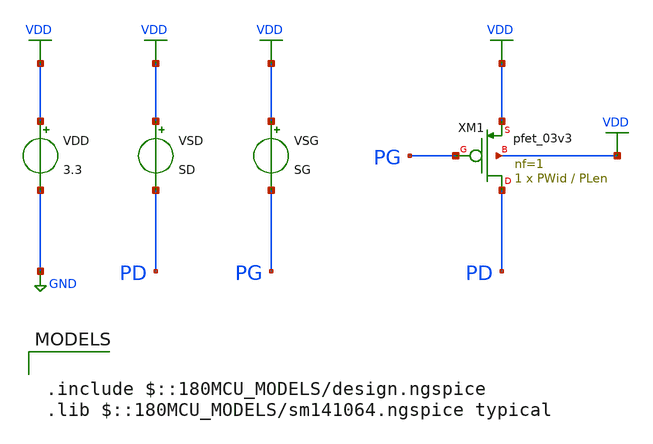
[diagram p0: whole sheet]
** sch_path: Design_Files/IC Design/Testbench/SIZING/Gm_Id/PMOS_Gm_Id.sch
**.subckt PMOS_Gm_Id
XM1 PD PG VDD VDD pfet_03v3 L=PLen W=PWid nf=1 ad='int((nf+1)/2) * W/nf * 0.18u' as='int((nf+2)/2) * W/nf * 0.18u'
+ pd='2*int((nf+1)/2) * (W/nf + 0.18u)' ps='2*int((nf+2)/2) * (W/nf + 0.18u)' nrd='0.18u / W' nrs='0.18u / W'
+ sa=0 sb=0 sd=0 m=1
VSG VDD PG SG
VSD VDD PD SD
.save i(vsd)
VDD VDD GND 3.3
**** begin user architecture code



.param PWid=10u
.param PLen=1u
.param SG=0
.param SD=1.65

.control

shell mkdir -p
+ /foss/designs/ECG_Acquisition_IC/Measurement_Results/IC_Simulation/SIZING/Gm_Id/PMOS_Gm_Id/Results_txt

set wr_vecnames
set wr_singlescale

* =========================================================
* PMOS gm/Id + fT 2D DC sweep
* W fixed at 10u
* VSG: 0 to 3.3 V
* VSD: 0 to 3.3 V
* Export: VSG VSD ID ID/W gm gds Cgs Cgd Cgb Cgg fT
* =========================================================

alterparam PLen = 0.28u
reset
save v(vdd) v(pg) v(pd) vsd#branch @m.xm1.m0[gm] @m.xm1.m0[gds] @m.xm1.m0[cgs] @m.xm1.m0[cgd]
+ @m.xm1.m0[cgb]
dc VSG 0 3.3 0.01 VSD 0 3.3 0.05
let vsg_out = v(vdd)-v(pg)
let vsd_out = v(vdd)-v(pd)
let id = abs(vsd#branch)
let id_w = id/10e-6
let gm = abs(@m.xm1.m0[gm])
let gds = abs(@m.xm1.m0[gds])
let cgs = abs(@m.xm1.m0[cgs])
let cgd = abs(@m.xm1.m0[cgd])
let cgb = abs(@m.xm1.m0[cgb])
let cgg = cgs + cgd + cgb
let ft_hz = gm/(6.283185307179586*(cgg + 1e-30))
let ft_mhz = ft_hz/1e6
wrdata
+ /foss/designs/ECG_Acquisition_IC/Measurement_Results/IC_Simulation/SIZING/Gm_Id/PMOS_Gm_Id/Results_txt/pmos_L0p28u_W10u.txt vsg_out vsd_out id id_w gm gds cgs cgd cgb cgg ft_hz ft_mhz

alterparam PLen = 0.5u
reset
save v(vdd) v(pg) v(pd) vsd#branch @m.xm1.m0[gm] @m.xm1.m0[gds] @m.xm1.m0[cgs] @m.xm1.m0[cgd]
+ @m.xm1.m0[cgb]
dc VSG 0 3.3 0.01 VSD 0 3.3 0.05
let vsg_out = v(vdd)-v(pg)
let vsd_out = v(vdd)-v(pd)
let id = abs(vsd#branch)
let id_w = id/10e-6
let gm = abs(@m.xm1.m0[gm])
let gds = abs(@m.xm1.m0[gds])
let cgs = abs(@m.xm1.m0[cgs])
let cgd = abs(@m.xm1.m0[cgd])
let cgb = abs(@m.xm1.m0[cgb])
let cgg = cgs + cgd + cgb
let ft_hz = gm/(6.283185307179586*(cgg + 1e-30))
let ft_mhz = ft_hz/1e6
wrdata
+ /foss/designs/ECG_Acquisition_IC/Measurement_Results/IC_Simulation/SIZING/Gm_Id/PMOS_Gm_Id/Results_txt/pmos_L0p5u_W10u.txt vsg_out vsd_out id id_w gm gds cgs cgd cgb cgg ft_hz ft_mhz

alterparam PLen = 1u
reset
save v(vdd) v(pg) v(pd) vsd#branch @m.xm1.m0[gm] @m.xm1.m0[gds] @m.xm1.m0[cgs] @m.xm1.m0[cgd]
+ @m.xm1.m0[cgb]
dc VSG 0 3.3 0.01 VSD 0 3.3 0.05
let vsg_out = v(vdd)-v(pg)
let vsd_out = v(vdd)-v(pd)
let id = abs(vsd#branch)
let id_w = id/10e-6
let gm = abs(@m.xm1.m0[gm])
let gds = abs(@m.xm1.m0[gds])
let cgs = abs(@m.xm1.m0[cgs])
let cgd = abs(@m.xm1.m0[cgd])
let cgb = abs(@m.xm1.m0[cgb])
let cgg = cgs + cgd + cgb
let ft_hz = gm/(6.283185307179586*(cgg + 1e-30))
let ft_mhz = ft_hz/1e6
wrdata
+ /foss/designs/ECG_Acquisition_IC/Measurement_Results/IC_Simulation/SIZING/Gm_Id/PMOS_Gm_Id/Results_txt/pmos_L1u_W10u.txt vsg_out vsd_out id id_w gm gds cgs cgd cgb cgg ft_hz ft_mhz

alterparam PLen = 1.5u
reset
save v(vdd) v(pg) v(pd) vsd#branch @m.xm1.m0[gm] @m.xm1.m0[gds] @m.xm1.m0[cgs] @m.xm1.m0[cgd]
+ @m.xm1.m0[cgb]
dc VSG 0 3.3 0.01 VSD 0 3.3 0.05
let vsg_out = v(vdd)-v(pg)
let vsd_out = v(vdd)-v(pd)
let id = abs(vsd#branch)
let id_w = id/10e-6
let gm = abs(@m.xm1.m0[gm])
let gds = abs(@m.xm1.m0[gds])
let cgs = abs(@m.xm1.m0[cgs])
let cgd = abs(@m.xm1.m0[cgd])
let cgb = abs(@m.xm1.m0[cgb])
let cgg = cgs + cgd + cgb
let ft_hz = gm/(6.283185307179586*(cgg + 1e-30))
let ft_mhz = ft_hz/1e6
wrdata
+ /foss/designs/ECG_Acquisition_IC/Measurement_Results/IC_Simulation/SIZING/Gm_Id/PMOS_Gm_Id/Results_txt/pmos_L1p5u_W10u.txt vsg_out vsd_out id id_w gm gds cgs cgd cgb cgg ft_hz ft_mhz

alterparam PLen = 2u
reset
save v(vdd) v(pg) v(pd) vsd#branch @m.xm1.m0[gm] @m.xm1.m0[gds] @m.xm1.m0[cgs] @m.xm1.m0[cgd]
+ @m.xm1.m0[cgb]
dc VSG 0 3.3 0.01 VSD 0 3.3 0.05
let vsg_out = v(vdd)-v(pg)
let vsd_out = v(vdd)-v(pd)
let id = abs(vsd#branch)
let id_w = id/10e-6
let gm = abs(@m.xm1.m0[gm])
let gds = abs(@m.xm1.m0[gds])
let cgs = abs(@m.xm1.m0[cgs])
let cgd = abs(@m.xm1.m0[cgd])
let cgb = abs(@m.xm1.m0[cgb])
let cgg = cgs + cgd + cgb
let ft_hz = gm/(6.283185307179586*(cgg + 1e-30))
let ft_mhz = ft_hz/1e6
wrdata
+ /foss/designs/ECG_Acquisition_IC/Measurement_Results/IC_Simulation/SIZING/Gm_Id/PMOS_Gm_Id/Results_txt/pmos_L2u_W10u.txt vsg_out vsd_out id id_w gm gds cgs cgd cgb cgg ft_hz ft_mhz

alterparam PLen = 3u
reset
save v(vdd) v(pg) v(pd) vsd#branch @m.xm1.m0[gm] @m.xm1.m0[gds] @m.xm1.m0[cgs] @m.xm1.m0[cgd]
+ @m.xm1.m0[cgb]
dc VSG 0 3.3 0.01 VSD 0 3.3 0.05
let vsg_out = v(vdd)-v(pg)
let vsd_out = v(vdd)-v(pd)
let id = abs(vsd#branch)
let id_w = id/10e-6
let gm = abs(@m.xm1.m0[gm])
let gds = abs(@m.xm1.m0[gds])
let cgs = abs(@m.xm1.m0[cgs])
let cgd = abs(@m.xm1.m0[cgd])
let cgb = abs(@m.xm1.m0[cgb])
let cgg = cgs + cgd + cgb
let ft_hz = gm/(6.283185307179586*(cgg + 1e-30))
let ft_mhz = ft_hz/1e6
wrdata
+ /foss/designs/ECG_Acquisition_IC/Measurement_Results/IC_Simulation/SIZING/Gm_Id/PMOS_Gm_Id/Results_txt/pmos_L3u_W10u.txt vsg_out vsd_out id id_w gm gds cgs cgd cgb cgg ft_hz ft_mhz

alterparam PLen = 4u
reset
save v(vdd) v(pg) v(pd) vsd#branch @m.xm1.m0[gm] @m.xm1.m0[gds] @m.xm1.m0[cgs] @m.xm1.m0[cgd]
+ @m.xm1.m0[cgb]
dc VSG 0 3.3 0.01 VSD 0 3.3 0.05
let vsg_out = v(vdd)-v(pg)
let vsd_out = v(vdd)-v(pd)
let id = abs(vsd#branch)
let id_w = id/10e-6
let gm = abs(@m.xm1.m0[gm])
let gds = abs(@m.xm1.m0[gds])
let cgs = abs(@m.xm1.m0[cgs])
let cgd = abs(@m.xm1.m0[cgd])
let cgb = abs(@m.xm1.m0[cgb])
let cgg = cgs + cgd + cgb
let ft_hz = gm/(6.283185307179586*(cgg + 1e-30))
let ft_mhz = ft_hz/1e6
wrdata
+ /foss/designs/ECG_Acquisition_IC/Measurement_Results/IC_Simulation/SIZING/Gm_Id/PMOS_Gm_Id/Results_txt/pmos_L4u_W10u.txt vsg_out vsd_out id id_w gm gds cgs cgd cgb cgg ft_hz ft_mhz

alterparam PLen = 5u
reset
save v(vdd) v(pg) v(pd) vsd#branch @m.xm1.m0[gm] @m.xm1.m0[gds] @m.xm1.m0[cgs] @m.xm1.m0[cgd]
+ @m.xm1.m0[cgb]
dc VSG 0 3.3 0.01 VSD 0 3.3 0.05
let vsg_out = v(vdd)-v(pg)
let vsd_out = v(vdd)-v(pd)
let id = abs(vsd#branch)
let id_w = id/10e-6
let gm = abs(@m.xm1.m0[gm])
let gds = abs(@m.xm1.m0[gds])
let cgs = abs(@m.xm1.m0[cgs])
let cgd = abs(@m.xm1.m0[cgd])
let cgb = abs(@m.xm1.m0[cgb])
let cgg = cgs + cgd + cgb
let ft_hz = gm/(6.283185307179586*(cgg + 1e-30))
let ft_mhz = ft_hz/1e6
wrdata
+ /foss/designs/ECG_Acquisition_IC/Measurement_Results/IC_Simulation/SIZING/Gm_Id/PMOS_Gm_Id/Results_txt/pmos_L5u_W10u.txt vsg_out vsd_out id id_w gm gds cgs cgd cgb cgg ft_hz ft_mhz

.endc



.include $::180MCU_MODELS/design.ngspice
.lib $::180MCU_MODELS/sm141064.ngspice typical

**** end user architecture code
**.ends
.GLOBAL VDD
.GLOBAL GND
.end
